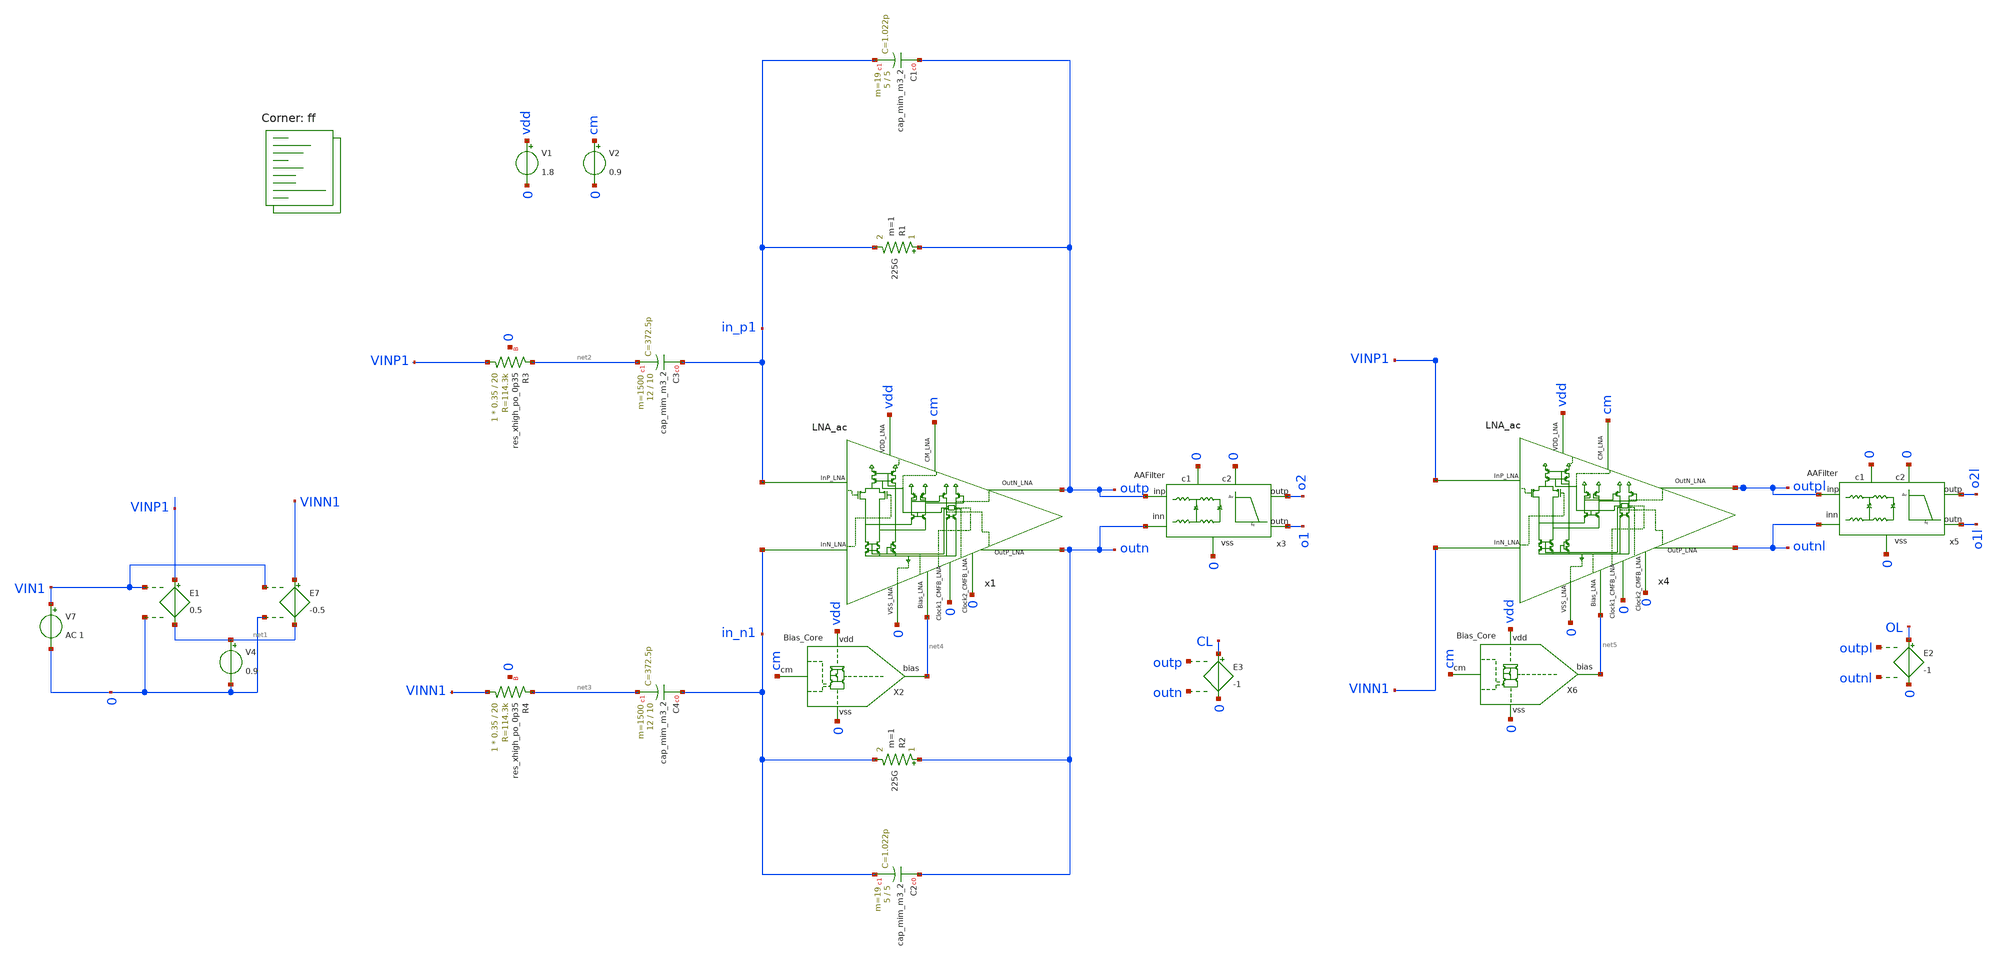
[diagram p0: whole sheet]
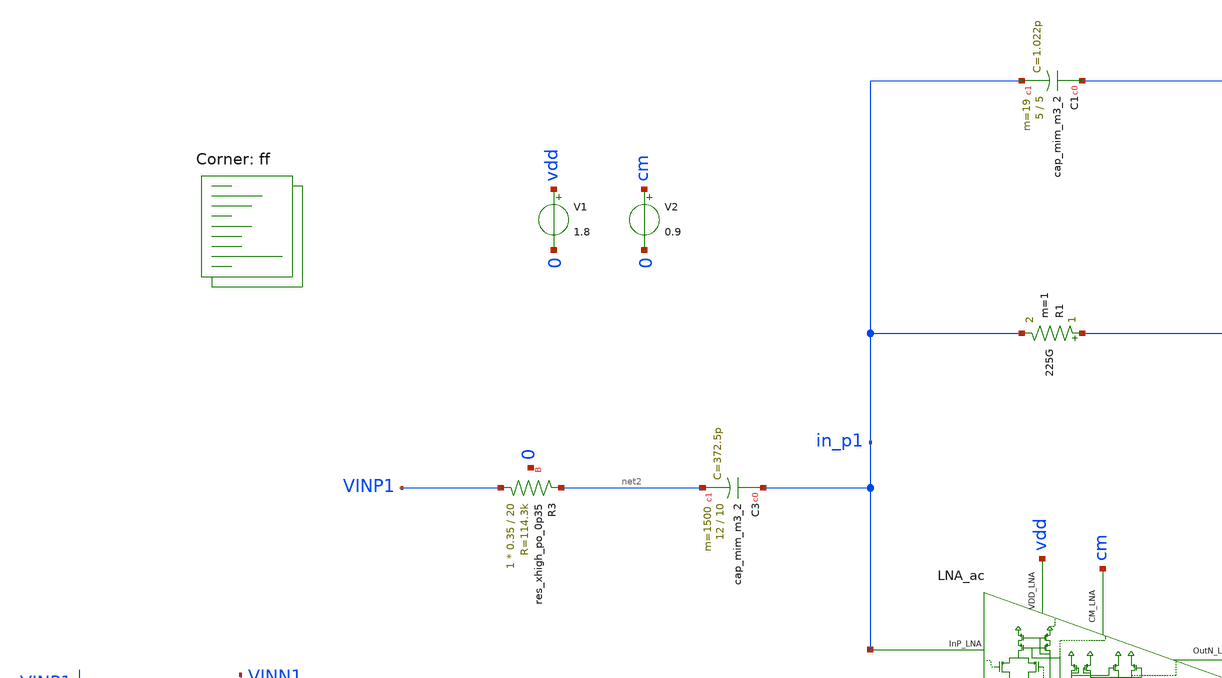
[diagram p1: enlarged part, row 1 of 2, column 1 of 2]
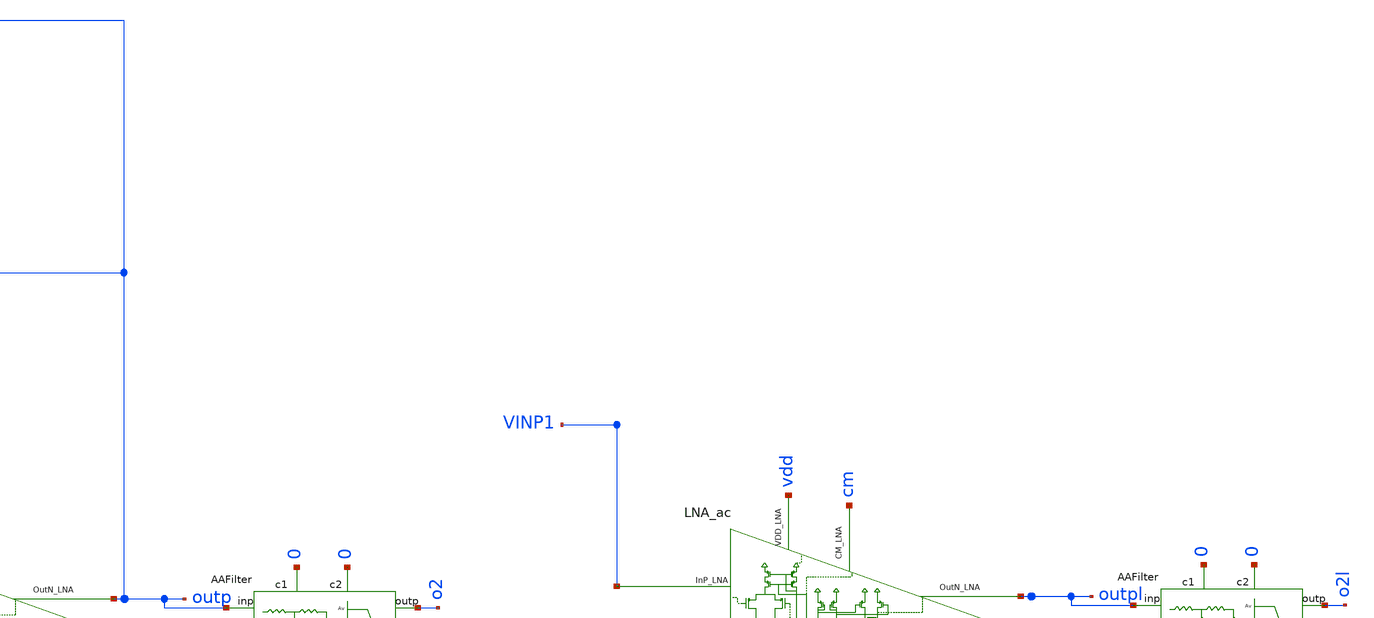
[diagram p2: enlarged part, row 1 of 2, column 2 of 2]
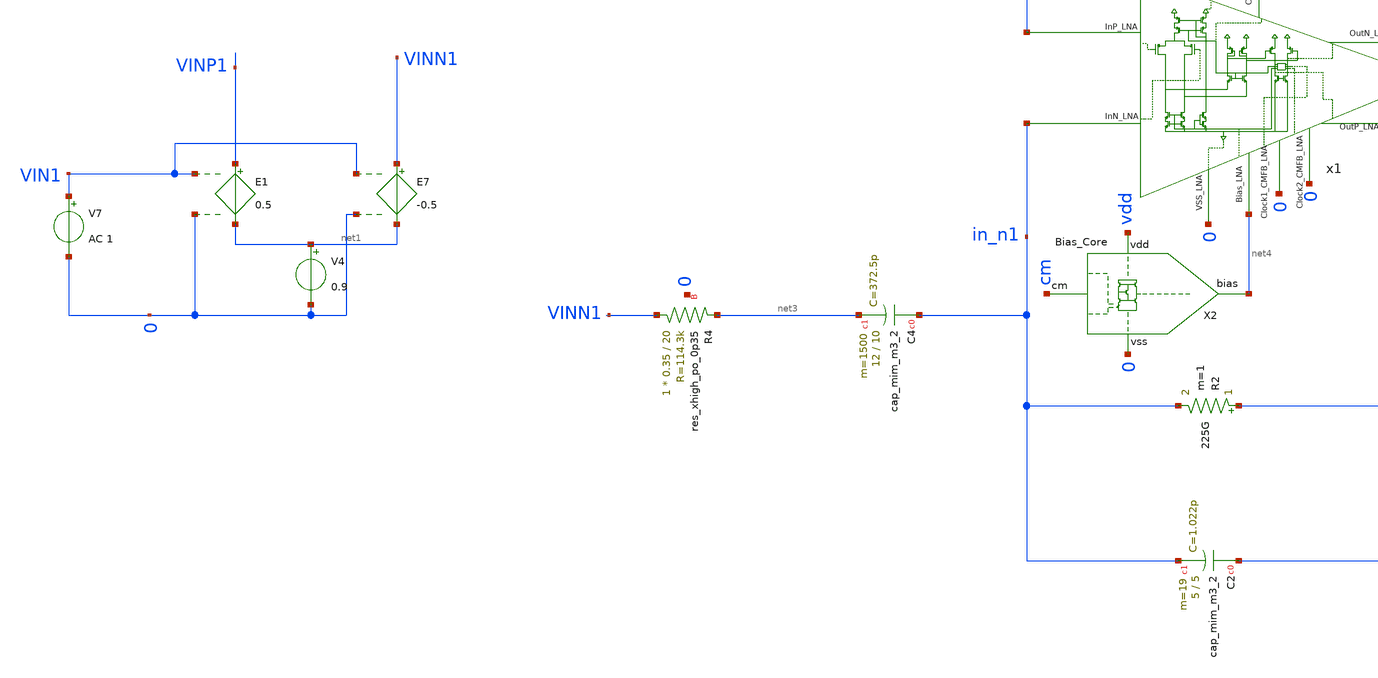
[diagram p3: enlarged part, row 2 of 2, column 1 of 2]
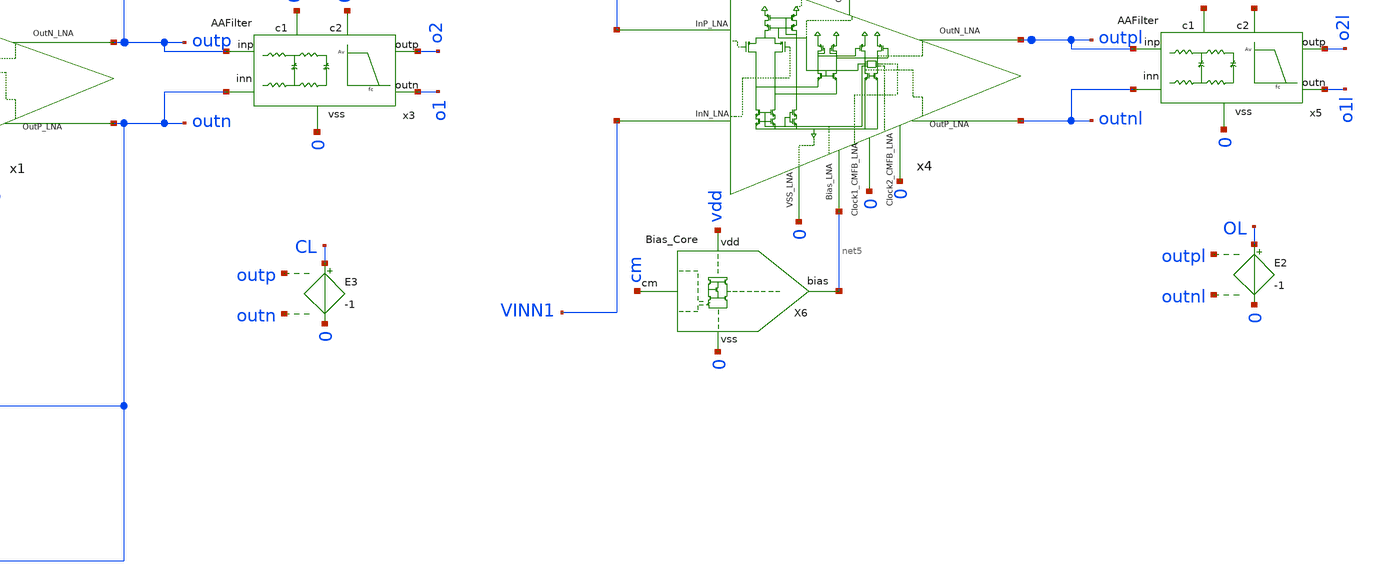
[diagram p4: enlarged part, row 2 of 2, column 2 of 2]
** sch_path: CL_Stability_b.sch
**.subckt CL_Stability_b
x1 in_n1 in_p1 vdd cm outp outn 0 net4 0 0 LNA_ac
V1 vdd 0 1.8
V2 cm 0 0.9
E1 VINP1 net1 VIN1 0 0.5
E7 VINN1 net1 VIN1 0 -0.5
V4 net1 0 0.9
V7 VIN1 0 AC 1
R1 outp in_p1 225G m=1
XC1 outp in_p1 sky130_fd_pr__cap_mim_m3_2 W=5 L=5 MF=19 m=19
XC2 outn in_n1 sky130_fd_pr__cap_mim_m3_2 W=5 L=5 MF=19 m=19
R2 outn in_n1 225G m=1
XC3 in_p1 net2 sky130_fd_pr__cap_mim_m3_2 W=12 L=10 MF=1500 m=1500
XC4 in_n1 net3 sky130_fd_pr__cap_mim_m3_2 W=12 L=10 MF=1500 m=1500
XR3 VINP1 net2 0 sky130_fd_pr__res_xhigh_po_0p35 L=20 mult=1 m=1
XR4 VINN1 net3 0 sky130_fd_pr__res_xhigh_po_0p35 L=20 mult=1 m=1
x3 outp outn o2 o1 0 0 0 AAFilter
X2 cm vdd 0 net4 Bias_Core
x4 VINN1 VINP1 vdd cm outpl outnl 0 net5 0 0 LNA_ac
x5 outpl outnl o2l o1l 0 0 0 AAFilter
X6 cm vdd 0 net5 Bias_Core
E2 OL 0 outpl outnl -1
E3 CL 0 outp outn -1
**** begin user architecture code
.lib $::SKYWATER_MODELS/sky130.lib.spice ff


.options savecurrents
*ic v(VM5)=0.9 v(VM6)=0.9
.control


save all

save @m.xm11.msky130_fd_pr__pfet_01v8_lvt[id]
save @m.xm11.msky130_fd_pr__pfet_01v8_lvt[vgs]


*nmos
save @m.xm3.msky130_fd_pr__nfet_01v8_lvt[vgs]
save @m.xm3.msky130_fd_pr__nfet_01v8_lvt[vth]
save @m.xm3.msky130_fd_pr__nfet_01v8_lvt[vds]

save @m.xm6.msky130_fd_pr__nfet_01v8_lvt[vgs]
save @m.xm6.msky130_fd_pr__nfet_01v8_lvt[vth]
save @m.xm6.msky130_fd_pr__nfet_01v8_lvt[vds]

save @m.xm8.msky130_fd_pr__nfet_01v8_lvt[vgs]
save @m.xm8.msky130_fd_pr__nfet_01v8_lvt[vth]
save @m.xm8.msky130_fd_pr__nfet_01v8_lvt[vds]

save @m.xm9.msky130_fd_pr__nfet_01v8_lvt[vgs]
save @m.xm9.msky130_fd_pr__nfet_01v8_lvt[vth]
save @m.xm9.msky130_fd_pr__nfet_01v8_lvt[vds]

save @m.xm18.msky130_fd_pr__nfet_01v8_lvt[vgs]
save @m.xm18.msky130_fd_pr__nfet_01v8_lvt[vth]
save @m.xm18.msky130_fd_pr__nfet_01v8_lvt[vds]

save @m.xm19.msky130_fd_pr__nfet_01v8_lvt[vgs]
save @m.xm19.msky130_fd_pr__nfet_01v8_lvt[vth]
save @m.xm19.msky130_fd_pr__nfet_01v8_lvt[vds]

save @m.xm25.msky130_fd_pr__nfet_01v8_lvt[vgs]
save @m.xm25.msky130_fd_pr__nfet_01v8_lvt[vth]
save @m.xm25.msky130_fd_pr__nfet_01v8_lvt[vds]

*pmos

save @m.xm1.msky130_fd_pr__pfet_01v8_lvt[vgs]
save @m.xm1.msky130_fd_pr__pfet_01v8_lvt[vth]
save @m.xm1.msky130_fd_pr__pfet_01v8_lvt[vds]


save @m.xm2.msky130_fd_pr__pfet_01v8_lvt[vgs]
save @m.xm2.msky130_fd_pr__pfet_01v8_lvt[vth]
save @m.xm2.msky130_fd_pr__pfet_01v8_lvt[vds]


save @m.xm10.msky130_fd_pr__pfet_01v8_lvt[vgs]
save @m.xm10.msky130_fd_pr__pfet_01v8_lvt[vth]
save @m.xm10.msky130_fd_pr__pfet_01v8_lvt[vds]

save @m.xm13.msky130_fd_pr__pfet_01v8_lvt[vgs]
save @m.xm13.msky130_fd_pr__pfet_01v8_lvt[vth]
save @m.xm13.msky130_fd_pr__pfet_01v8_lvt[vds]

save @m.xm4.msky130_fd_pr__pfet_01v8_lvt[vgs]
save @m.xm4.msky130_fd_pr__pfet_01v8_lvt[vth]
save @m.xm4.msky130_fd_pr__pfet_01v8_lvt[vds]

save @m.xm5.msky130_fd_pr__pfet_01v8_lvt[vgs]
save @m.xm5.msky130_fd_pr__pfet_01v8_lvt[vth]
save @m.xm5.msky130_fd_pr__pfet_01v8_lvt[vds]

save @m.xm16.msky130_fd_pr__pfet_01v8_lvt[vgs]
save @m.xm16.msky130_fd_pr__pfet_01v8_lvt[vth]
save @m.xm16.msky130_fd_pr__pfet_01v8_lvt[vds]

save @m.xm17.msky130_fd_pr__pfet_01v8_lvt[vgs]
save @m.xm17.msky130_fd_pr__pfet_01v8_lvt[vth]
save @m.xm17.msky130_fd_pr__pfet_01v8_lvt[vds]

save @m.xm3.msky130_fd_pr__pfet_01v8_lvt[vgs]
save @m.xm3.msky130_fd_pr__pfet_01v8_lvt[vth]
save @m.xm3.msky130_fd_pr__pfet_01v8_lvt[vds]

save @m.xm20.msky130_fd_pr__pfet_01v8_lvt[vgs]
save @m.xm20.msky130_fd_pr__pfet_01v8_lvt[vth]
save @m.xm20.msky130_fd_pr__pfet_01v8_lvt[vds]

save @m.xm2.msky130_fd_pr__pfet_01v8_lvt[vgs]
save @m.xm2.msky130_fd_pr__pfet_01v8_lvt[vth]
save @m.xm2.msky130_fd_pr__pfet_01v8_lvt[vds]

save @m.xm21.msky130_fd_pr__pfet_01v8_lvt[vgs]
save @m.xm21.msky130_fd_pr__pfet_01v8_lvt[vth]
save @m.xm21.msky130_fd_pr__pfet_01v8_lvt[vds]

save @m.xm7.msky130_fd_pr__nfet_01v8_lvt[vth]

save @m.xm1.msky130_fd_pr__pfet_01v8[vgs]

save @m.xm1.msky130_fd_pr__nfet_01v8_lvt[gm]


save @m.xm1.msky130_fd_pr__nfet_01v8_lvt[gds]
save @m.xm2.msky130_fd_pr__pfet_01v8_lvt[gm]

save @m.xm23.msky130_fd_pr__nfet_01v8[cgs]
save @m.xm4.msky130_fd_pr__pfet_01v8[cgs]
save @m.xm2.msky130_fd_pr__pfet_01v8_lvt[cgs]



save @m.xm2.msky130_fd_pr__pfet_01v8_lvt[gds]


op
write CL_ac.raw
*set appendwrite


.endc
.control



*tran 50u 1500m
*save all
*plot v(Outp)-v(outn)


noise V(Outp,Outn) V7 dec 100 0.1 128
print inoise_total onoise_total
setplot noise1
plot inoise_spectrum

ac dec 10 0.1 1000k
let gaind=(v(outp)-v(outn))/(v(in_p1)-v(in_n1))
let lg=vr/VIN1
let BG=(OL/CL)-1
let phase=180*cph(BG)/pi
plot db(gaind)
plot db(BG) phase


.endc






.include $::SKYWATER_STDCELLS/sky130_fd_sc_hd.spice

**** end user architecture code
**.ends

* expanding   symbol:  LNA/LNA_ac.sym # of pins=10
** sym_path: LNA_ac.sym
** sch_path: LNA_ac.sch
.subckt LNA_ac InN_LNA InP_LNA VDD_LNA CM_LNA OutN_LNA OutP_LNA VSS_LNA Bias_LNA Clock1_CMFB_LNA
+ Clock2_CMFB_LNA
*.iopin InP_LNA
*.iopin InN_LNA
*.iopin VSS_LNA
*.iopin VDD_LNA
*.iopin CM_LNA
*.opin OutP_LNA
*.opin OutN_LNA
*.iopin Clock2_CMFB_LNA
*.iopin Bias_LNA
*.iopin Clock1_CMFB_LNA
XM4 net3 InP_LNA VT2 VT2 sky130_fd_pr__pfet_01v8_lvt L=10 W=90 nf=1 ad='int((nf+1)/2) * W/nf * 0.29'
+ as='int((nf+2)/2) * W/nf * 0.29' pd='2*int((nf+1)/2) * (W/nf + 0.29)' ps='2*int((nf+2)/2) * (W/nf + 0.29)'
+ nrd='0.29 / W' nrs='0.29 / W' sa=0 sb=0 sd=0 mult=5 m=5
XM5 net2 InN_LNA VT2 VT2 sky130_fd_pr__pfet_01v8_lvt L=10 W=90 nf=1 ad='int((nf+1)/2) * W/nf * 0.29'
+ as='int((nf+2)/2) * W/nf * 0.29' pd='2*int((nf+1)/2) * (W/nf + 0.29)' ps='2*int((nf+2)/2) * (W/nf + 0.29)'
+ nrd='0.29 / W' nrs='0.29 / W' sa=0 sb=0 sd=0 mult=5 m=5
XM8 net3 Bias_LNA VSS_LNA VSS_LNA sky130_fd_pr__nfet_01v8_lvt L=20 W=10 nf=1 ad='int((nf+1)/2) * W/nf * 0.29'
+ as='int((nf+2)/2) * W/nf * 0.29' pd='2*int((nf+1)/2) * (W/nf + 0.29)' ps='2*int((nf+2)/2) * (W/nf + 0.29)'
+ nrd='0.29 / W' nrs='0.29 / W' sa=0 sb=0 sd=0 mult=4 m=4
XM9 net2 Bias_LNA VSS_LNA VSS_LNA sky130_fd_pr__nfet_01v8_lvt L=20 W=10 nf=1 ad='int((nf+1)/2) * W/nf * 0.29'
+ as='int((nf+2)/2) * W/nf * 0.29' pd='2*int((nf+1)/2) * (W/nf + 0.29)' ps='2*int((nf+2)/2) * (W/nf + 0.29)'
+ nrd='0.29 / W' nrs='0.29 / W' sa=0 sb=0 sd=0 mult=4 m=4
XM16 b b VDD_LNA VDD_LNA sky130_fd_pr__pfet_01v8_lvt L=20 W=6 nf=1 ad='int((nf+1)/2) * W/nf * 0.29' as='int((nf+2)/2) * W/nf * 0.29'
+ pd='2*int((nf+1)/2) * (W/nf + 0.29)' ps='2*int((nf+2)/2) * (W/nf + 0.29)' nrd='0.29 / W' nrs='0.29 / W'
+ sa=0 sb=0 sd=0 mult=1 m=1
XM17 a a VDD_LNA VDD_LNA sky130_fd_pr__pfet_01v8_lvt L=20 W=6 nf=1 ad='int((nf+1)/2) * W/nf * 0.29' as='int((nf+2)/2) * W/nf * 0.29'
+ pd='2*int((nf+1)/2) * (W/nf + 0.29)' ps='2*int((nf+2)/2) * (W/nf + 0.29)' nrd='0.29 / W' nrs='0.29 / W'
+ sa=0 sb=0 sd=0 mult=1 m=1
XM18 b CM_LNA net2 VSS_LNA sky130_fd_pr__nfet_01v8_lvt L=20 W=1 nf=1 ad='int((nf+1)/2) * W/nf * 0.29'
+ as='int((nf+2)/2) * W/nf * 0.29' pd='2*int((nf+1)/2) * (W/nf + 0.29)' ps='2*int((nf+2)/2) * (W/nf + 0.29)'
+ nrd='0.29 / W' nrs='0.29 / W' sa=0 sb=0 sd=0 mult=1 m=1
XM19 a CM_LNA net3 VSS_LNA sky130_fd_pr__nfet_01v8_lvt L=20 W=1 nf=1 ad='int((nf+1)/2) * W/nf * 0.29'
+ as='int((nf+2)/2) * W/nf * 0.29' pd='2*int((nf+1)/2) * (W/nf + 0.29)' ps='2*int((nf+2)/2) * (W/nf + 0.29)'
+ nrd='0.29 / W' nrs='0.29 / W' sa=0 sb=0 sd=0 mult=1 m=1
XM20 OutP_LNA a VDD_LNA VDD_LNA sky130_fd_pr__pfet_01v8_lvt L=20 W=6 nf=1 ad='int((nf+1)/2) * W/nf * 0.29'
+ as='int((nf+2)/2) * W/nf * 0.29' pd='2*int((nf+1)/2) * (W/nf + 0.29)' ps='2*int((nf+2)/2) * (W/nf + 0.29)'
+ nrd='0.29 / W' nrs='0.29 / W' sa=0 sb=0 sd=0 mult=10 m=10
XM21 OutN_LNA b VDD_LNA VDD_LNA sky130_fd_pr__pfet_01v8_lvt L=20 W=6 nf=1 ad='int((nf+1)/2) * W/nf * 0.29'
+ as='int((nf+2)/2) * W/nf * 0.29' pd='2*int((nf+1)/2) * (W/nf + 0.29)' ps='2*int((nf+2)/2) * (W/nf + 0.29)'
+ nrd='0.29 / W' nrs='0.29 / W' sa=0 sb=0 sd=0 mult=10 m=10
XM23 OutN_LNA cmvo VSS_LNA VSS_LNA sky130_fd_pr__nfet_01v8_lvt L=20 W=10 nf=1 ad='int((nf+1)/2) * W/nf * 0.29'
+ as='int((nf+2)/2) * W/nf * 0.29' pd='2*int((nf+1)/2) * (W/nf + 0.29)' ps='2*int((nf+2)/2) * (W/nf + 0.29)'
+ nrd='0.29 / W' nrs='0.29 / W' sa=0 sb=0 sd=0 mult=10 m=10
XM25 OutP_LNA cmvo VSS_LNA VSS_LNA sky130_fd_pr__nfet_01v8_lvt L=20 W=10 nf=1 ad='int((nf+1)/2) * W/nf * 0.29'
+ as='int((nf+2)/2) * W/nf * 0.29' pd='2*int((nf+1)/2) * (W/nf + 0.29)' ps='2*int((nf+2)/2) * (W/nf + 0.29)'
+ nrd='0.29 / W' nrs='0.29 / W' sa=0 sb=0 sd=0 mult=10 m=10
XM2 VT2 net1 VDD_LNA VDD_LNA sky130_fd_pr__pfet_01v8_lvt L=20 W=2 nf=1 ad='int((nf+1)/2) * W/nf * 0.29'
+ as='int((nf+2)/2) * W/nf * 0.29' pd='2*int((nf+1)/2) * (W/nf + 0.29)' ps='2*int((nf+2)/2) * (W/nf + 0.29)'
+ nrd='0.29 / W' nrs='0.29 / W' sa=0 sb=0 sd=0 mult=6 m=6
XM3 net1 net1 VDD_LNA VDD_LNA sky130_fd_pr__pfet_01v8_lvt L=20 W=2 nf=1 ad='int((nf+1)/2) * W/nf * 0.29'
+ as='int((nf+2)/2) * W/nf * 0.29' pd='2*int((nf+1)/2) * (W/nf + 0.29)' ps='2*int((nf+2)/2) * (W/nf + 0.29)'
+ nrd='0.29 / W' nrs='0.29 / W' sa=0 sb=0 sd=0 mult=1 m=1
XM6 net1 Bias_LNA VSS_LNA VSS_LNA sky130_fd_pr__nfet_01v8_lvt L=20 W=10 nf=1 ad='int((nf+1)/2) * W/nf * 0.29'
+ as='int((nf+2)/2) * W/nf * 0.29' pd='2*int((nf+1)/2) * (W/nf + 0.29)' ps='2*int((nf+2)/2) * (W/nf + 0.29)'
+ nrd='0.29 / W' nrs='0.29 / W' sa=0 sb=0 sd=0 mult=1 m=1
E3 f1 VSS_LNA OutN_LNA VSS_LNA -1
E4 f2 VSS_LNA OutP_LNA f1 1
E5 f3 VSS_LNA f2 VSS_LNA 0.5
E6 cmvo VSS_LNA CM_LNA f3 {-1000}
XC1 OutP_LNA a sky130_fd_pr__cap_mim_m3_2 W=12 L=10 MF=32 m=32
XC2 OutN_LNA b sky130_fd_pr__cap_mim_m3_2 W=12 L=10 MF=32 m=32
.ends


* expanding   symbol:  LNA/AAFilter.sym # of pins=7
** sym_path: AAFilter.sym
** sch_path: AAFilter.sch
.subckt AAFilter inp inn outp outn c1 c2 vss
*.iopin inp
*.iopin inn
*.iopin vss
*.opin outp
*.opin outn
*.iopin c1
*.iopin c2
XR4 inp net3 vss sky130_fd_pr__res_xhigh_po_0p35 L=95 mult=1 m=1
XR15 net3 net1 vss sky130_fd_pr__res_xhigh_po_0p35 L=95 mult=1 m=1
XR16 net1 net4 vss sky130_fd_pr__res_xhigh_po_0p35 L=95 mult=1 m=1
XR17 net4 outp vss sky130_fd_pr__res_xhigh_po_0p35 L=95 mult=1 m=1
XR19 net2 net5 vss sky130_fd_pr__res_xhigh_po_0p35 L=95 mult=1 m=1
XR20 net5 inn vss sky130_fd_pr__res_xhigh_po_0p35 L=95 mult=1 m=1
XR23 outn net6 vss sky130_fd_pr__res_xhigh_po_0p35 L=95 mult=1 m=1
XR24 net6 net2 vss sky130_fd_pr__res_xhigh_po_0p35 L=95 mult=1 m=1
XC4 net1 net2 sky130_fd_pr__cap_mim_m3_1 W=15 L=10 MF=30 m=30
XC5 outp outn sky130_fd_pr__cap_mim_m3_1 W=15 L=10 MF=30 m=30
.ends


* expanding   symbol:  LNA/Bias_Core.sym # of pins=4
** sym_path: Bias_Core.sym
** sch_path: Bias_Core.sch
.subckt Bias_Core cm vdd vss bias
*.ipin vdd
*.ipin vss
*.opin bias
*.ipin cm
XM7 net3 bias vss vss sky130_fd_pr__nfet_01v8_lvt L=20 W=10 nf=1 ad='int((nf+1)/2) * W/nf * 0.29' as='int((nf+2)/2) * W/nf * 0.29'
+ pd='2*int((nf+1)/2) * (W/nf + 0.29)' ps='2*int((nf+2)/2) * (W/nf + 0.29)' nrd='0.29 / W' nrs='0.29 / W'
+ sa=0 sb=0 sd=0 mult=1 m=1
XM10 net4 vx vr vdd sky130_fd_pr__pfet_01v8_lvt L=20 W=10 nf=1 ad='int((nf+1)/2) * W/nf * 0.29' as='int((nf+2)/2) * W/nf * 0.29'
+ pd='2*int((nf+1)/2) * (W/nf + 0.29)' ps='2*int((nf+2)/2) * (W/nf + 0.29)' nrd='0.29 / W' nrs='0.29 / W'
+ sa=0 sb=0 sd=0 mult=30 m=30
XM11 bias cm net3 vss sky130_fd_pr__nfet_01v8_lvt L=1 W=10 nf=1 ad='int((nf+1)/2) * W/nf * 0.29' as='int((nf+2)/2) * W/nf * 0.29'
+ pd='2*int((nf+1)/2) * (W/nf + 0.29)' ps='2*int((nf+2)/2) * (W/nf + 0.29)' nrd='0.29 / W' nrs='0.29 / W'
+ sa=0 sb=0 sd=0 mult=40 m=40
XM12 net2 bias vss vss sky130_fd_pr__nfet_01v8_lvt L=20 W=10 nf=1 ad='int((nf+1)/2) * W/nf * 0.29' as='int((nf+2)/2) * W/nf * 0.29'
+ pd='2*int((nf+1)/2) * (W/nf + 0.29)' ps='2*int((nf+2)/2) * (W/nf + 0.29)' nrd='0.29 / W' nrs='0.29 / W'
+ sa=0 sb=0 sd=0 mult=1 m=1
XM13 vx cm net2 vss sky130_fd_pr__nfet_01v8_lvt L=1 W=10 nf=1 ad='int((nf+1)/2) * W/nf * 0.29' as='int((nf+2)/2) * W/nf * 0.29'
+ pd='2*int((nf+1)/2) * (W/nf + 0.29)' ps='2*int((nf+2)/2) * (W/nf + 0.29)' nrd='0.29 / W' nrs='0.29 / W'
+ sa=0 sb=0 sd=0 mult=40 m=40
XM2 net8 vx net1 vdd sky130_fd_pr__pfet_01v8_lvt L=20 W=10 nf=1 ad='int((nf+1)/2) * W/nf * 0.29' as='int((nf+2)/2) * W/nf * 0.29'
+ pd='2*int((nf+1)/2) * (W/nf + 0.29)' ps='2*int((nf+2)/2) * (W/nf + 0.29)' nrd='0.29 / W' nrs='0.29 / W'
+ sa=0 sb=0 sd=0 mult=30 m=30
XM3 net1 net1 vdd vdd sky130_fd_pr__pfet_01v8_lvt L=20 W=10 nf=1 ad='int((nf+1)/2) * W/nf * 0.29' as='int((nf+2)/2) * W/nf * 0.29'
+ pd='2*int((nf+1)/2) * (W/nf + 0.29)' ps='2*int((nf+2)/2) * (W/nf + 0.29)' nrd='0.29 / W' nrs='0.29 / W'
+ sa=0 sb=0 sd=0 mult=1 m=1
XM4 net5 net5 bias vss sky130_fd_pr__nfet_01v8_lvt L=10 W=1 nf=1 ad='int((nf+1)/2) * W/nf * 0.29' as='int((nf+2)/2) * W/nf * 0.29'
+ pd='2*int((nf+1)/2) * (W/nf + 0.29)' ps='2*int((nf+2)/2) * (W/nf + 0.29)' nrd='0.29 / W' nrs='0.29 / W'
+ sa=0 sb=0 sd=0 mult=1 m=1
XM5 net6 net6 net5 vss sky130_fd_pr__nfet_01v8_lvt L=10 W=1 nf=1 ad='int((nf+1)/2) * W/nf * 0.29' as='int((nf+2)/2) * W/nf * 0.29'
+ pd='2*int((nf+1)/2) * (W/nf + 0.29)' ps='2*int((nf+2)/2) * (W/nf + 0.29)' nrd='0.29 / W' nrs='0.29 / W'
+ sa=0 sb=0 sd=0 mult=1 m=1
XM8 net7 net7 net6 vss sky130_fd_pr__nfet_01v8_lvt L=10 W=1 nf=1 ad='int((nf+1)/2) * W/nf * 0.29' as='int((nf+2)/2) * W/nf * 0.29'
+ pd='2*int((nf+1)/2) * (W/nf + 0.29)' ps='2*int((nf+2)/2) * (W/nf + 0.29)' nrd='0.29 / W' nrs='0.29 / W'
+ sa=0 sb=0 sd=0 mult=1 m=1
XM9 vx vx net7 vss sky130_fd_pr__nfet_01v8_lvt L=10 W=1 nf=1 ad='int((nf+1)/2) * W/nf * 0.29' as='int((nf+2)/2) * W/nf * 0.29'
+ pd='2*int((nf+1)/2) * (W/nf + 0.29)' ps='2*int((nf+2)/2) * (W/nf + 0.29)' nrd='0.29 / W' nrs='0.29 / W'
+ sa=0 sb=0 sd=0 mult=1 m=1
XM23 bias vx net4 vdd sky130_fd_pr__pfet_01v8_lvt L=20 W=10 nf=1 ad='int((nf+1)/2) * W/nf * 0.29' as='int((nf+2)/2) * W/nf * 0.29'
+ pd='2*int((nf+1)/2) * (W/nf + 0.29)' ps='2*int((nf+2)/2) * (W/nf + 0.29)' nrd='0.29 / W' nrs='0.29 / W'
+ sa=0 sb=0 sd=0 mult=8 m=8
XM24 vx vx net8 vdd sky130_fd_pr__pfet_01v8_lvt L=20 W=10 nf=1 ad='int((nf+1)/2) * W/nf * 0.29' as='int((nf+2)/2) * W/nf * 0.29'
+ pd='2*int((nf+1)/2) * (W/nf + 0.29)' ps='2*int((nf+2)/2) * (W/nf + 0.29)' nrd='0.29 / W' nrs='0.29 / W'
+ sa=0 sb=0 sd=0 mult=8 m=8
R27 vdd vr 7e6 m=1
.ends

.end
